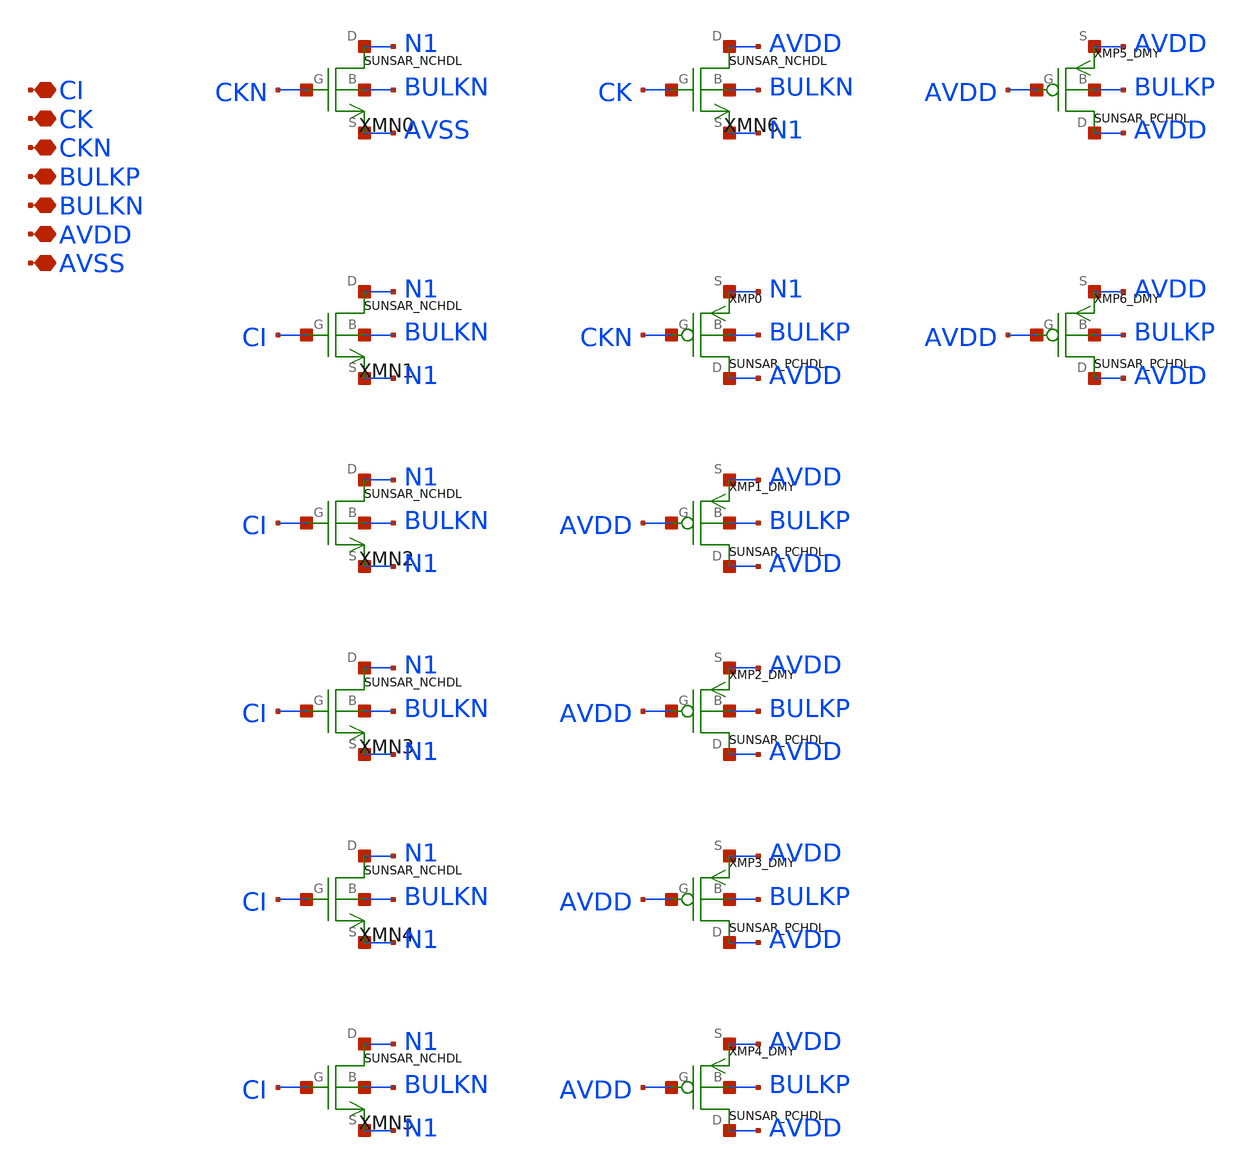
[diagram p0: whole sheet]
** sch_path: ip/sun_sar9b_sky130nm/design/SUN_SAR9B_SKY130NM/SUNSAR_SARKICKHX1_CV.sch
**.subckt SUNSAR_SARKICKHX1_CV CI CK CKN BULKP BULKN AVDD AVSS
*.iopin CI
*.iopin CK
*.iopin CKN
*.iopin BULKP
*.iopin BULKN
*.iopin AVDD
*.iopin AVSS
XMN0 N1 CKN AVSS BULKN SUNSAR_NCHDL
XMN1 N1 CI N1 BULKN SUNSAR_NCHDL
XMN2 N1 CI N1 BULKN SUNSAR_NCHDL
XMN3 N1 CI N1 BULKN SUNSAR_NCHDL
XMN4 N1 CI N1 BULKN SUNSAR_NCHDL
XMN5 N1 CI N1 BULKN SUNSAR_NCHDL
XMN6 AVDD CK N1 BULKN SUNSAR_NCHDL
XMP0 AVDD CKN N1 BULKP SUNSAR_PCHDL
XMP1_DMY AVDD AVDD AVDD BULKP SUNSAR_PCHDL
XMP2_DMY AVDD AVDD AVDD BULKP SUNSAR_PCHDL
XMP3_DMY AVDD AVDD AVDD BULKP SUNSAR_PCHDL
XMP4_DMY AVDD AVDD AVDD BULKP SUNSAR_PCHDL
XMP5_DMY AVDD AVDD AVDD BULKP SUNSAR_PCHDL
XMP6_DMY AVDD AVDD AVDD BULKP SUNSAR_PCHDL
**.ends
.end
